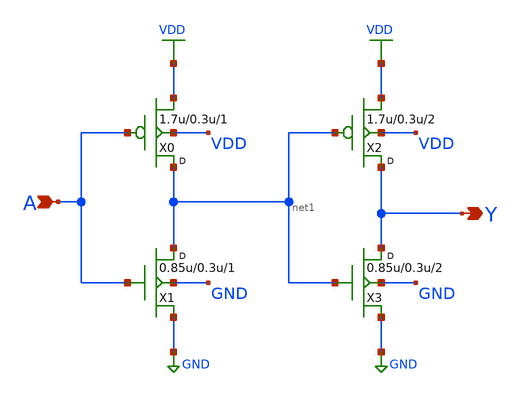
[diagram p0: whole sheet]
** sch_path: lib/9T/schematics/gf180mcu_osu_sc_buf_2.sch
**.subckt gf180mcu_osu_sc_buf_2 A Y
*.ipin A
*.opin Y
X0 net1 A VDD VDD pmos_3p3 w=1.7u l=0.3u m=1
X1 net1 A GND GND nmos_3p3 w=0.85u l=0.3u m=1
X2 Y net1 VDD VDD pmos_3p3 w=1.7u l=0.3u m=2
X3 Y net1 GND GND nmos_3p3 w=0.85u l=0.3u m=2
**** begin user architecture code


.inc "/import/yukari1/lrburle/OSU_180/char/techfiles/design.hspice"
.lib "/import/yukari1/lrburle/OSU_180/char/techfiles/sm141064.hspice" typical


**** end user architecture code
**.ends
.GLOBAL VDD
.GLOBAL GND
.end
